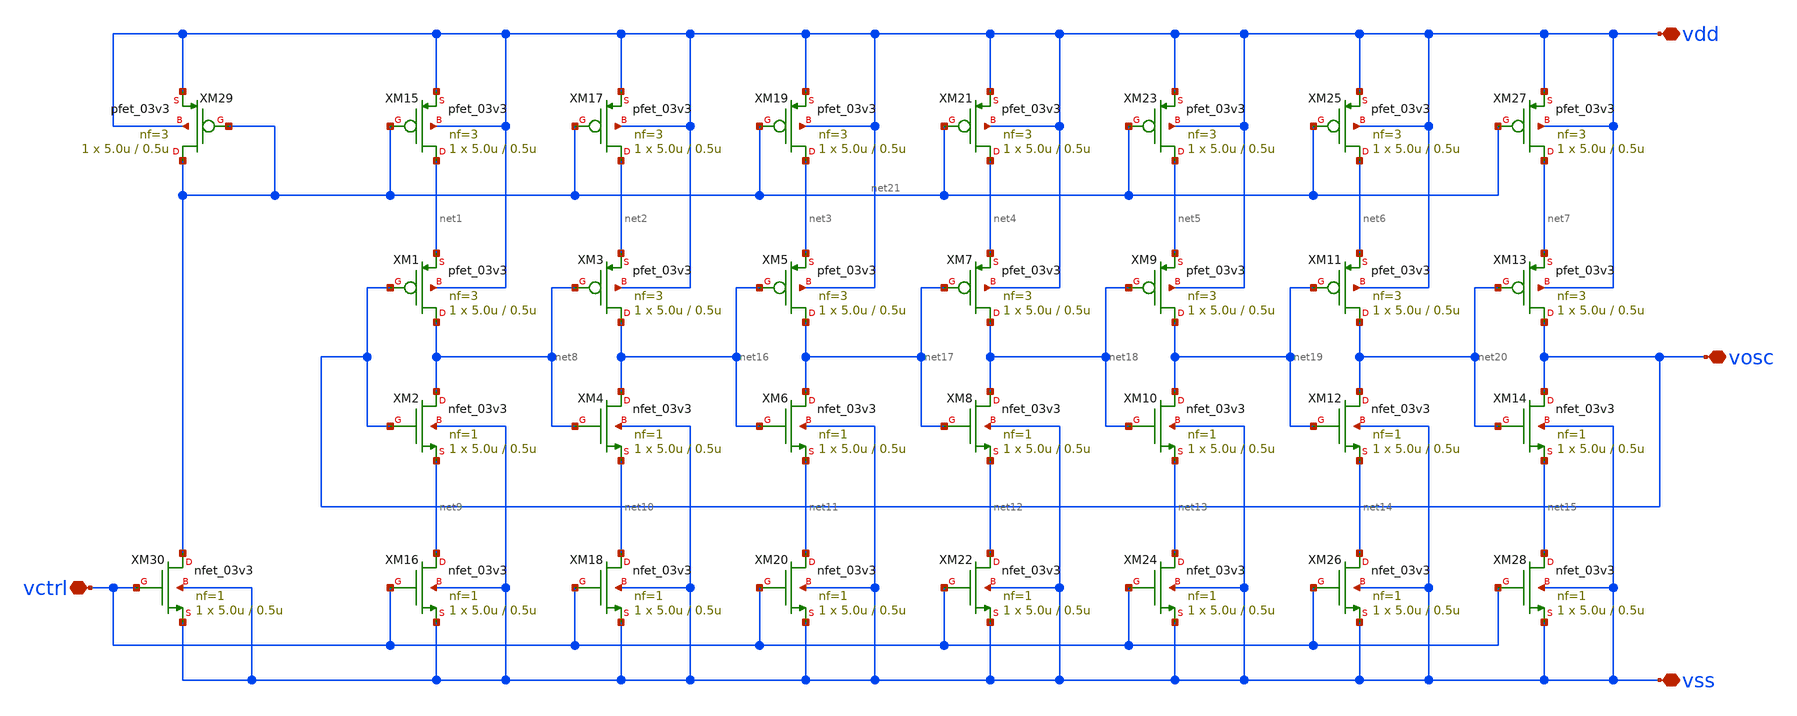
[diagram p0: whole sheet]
** sch_path: designs/libs/core_analog/CSRVCO/CSRVCO.sch
**.subckt CSRVCO vctrl vdd vss vosc
*.iopin vctrl
*.iopin vdd
*.iopin vss
*.iopin vosc
XM1 net8 vosc net1 vdd pfet_03v3 L=0.5u W=5.0u nf=3 ad='int((nf+1)/2) * W/nf * 0.18u' as='int((nf+2)/2) * W/nf * 0.18u'
+ pd='2*int((nf+1)/2) * (W/nf + 0.18u)' ps='2*int((nf+2)/2) * (W/nf + 0.18u)' nrd='0.18u / W' nrs='0.18u / W'
+ sa=0 sb=0 sd=0 m=1
XM2 net8 vosc net9 vss nfet_03v3 L=0.5u W=5.0u nf=1 ad='int((nf+1)/2) * W/nf * 0.18u' as='int((nf+2)/2) * W/nf * 0.18u'
+ pd='2*int((nf+1)/2) * (W/nf + 0.18u)' ps='2*int((nf+2)/2) * (W/nf + 0.18u)' nrd='0.18u / W' nrs='0.18u / W'
+ sa=0 sb=0 sd=0 m=1
XM3 net16 net8 net2 vdd pfet_03v3 L=0.5u W=5.0u nf=3 ad='int((nf+1)/2) * W/nf * 0.18u' as='int((nf+2)/2) * W/nf * 0.18u'
+ pd='2*int((nf+1)/2) * (W/nf + 0.18u)' ps='2*int((nf+2)/2) * (W/nf + 0.18u)' nrd='0.18u / W' nrs='0.18u / W'
+ sa=0 sb=0 sd=0 m=1
XM4 net16 net8 net10 vss nfet_03v3 L=0.5u W=5.0u nf=1 ad='int((nf+1)/2) * W/nf * 0.18u' as='int((nf+2)/2) * W/nf * 0.18u'
+ pd='2*int((nf+1)/2) * (W/nf + 0.18u)' ps='2*int((nf+2)/2) * (W/nf + 0.18u)' nrd='0.18u / W' nrs='0.18u / W'
+ sa=0 sb=0 sd=0 m=1
XM5 net17 net16 net3 vdd pfet_03v3 L=0.5u W=5.0u nf=3 ad='int((nf+1)/2) * W/nf * 0.18u' as='int((nf+2)/2) * W/nf * 0.18u'
+ pd='2*int((nf+1)/2) * (W/nf + 0.18u)' ps='2*int((nf+2)/2) * (W/nf + 0.18u)' nrd='0.18u / W' nrs='0.18u / W'
+ sa=0 sb=0 sd=0 m=1
XM6 net17 net16 net11 vss nfet_03v3 L=0.5u W=5.0u nf=1 ad='int((nf+1)/2) * W/nf * 0.18u' as='int((nf+2)/2) * W/nf * 0.18u'
+ pd='2*int((nf+1)/2) * (W/nf + 0.18u)' ps='2*int((nf+2)/2) * (W/nf + 0.18u)' nrd='0.18u / W' nrs='0.18u / W'
+ sa=0 sb=0 sd=0 m=1
XM7 net18 net17 net4 vdd pfet_03v3 L=0.5u W=5.0u nf=3 ad='int((nf+1)/2) * W/nf * 0.18u' as='int((nf+2)/2) * W/nf * 0.18u'
+ pd='2*int((nf+1)/2) * (W/nf + 0.18u)' ps='2*int((nf+2)/2) * (W/nf + 0.18u)' nrd='0.18u / W' nrs='0.18u / W'
+ sa=0 sb=0 sd=0 m=1
XM8 net18 net17 net12 vss nfet_03v3 L=0.5u W=5.0u nf=1 ad='int((nf+1)/2) * W/nf * 0.18u' as='int((nf+2)/2) * W/nf * 0.18u'
+ pd='2*int((nf+1)/2) * (W/nf + 0.18u)' ps='2*int((nf+2)/2) * (W/nf + 0.18u)' nrd='0.18u / W' nrs='0.18u / W'
+ sa=0 sb=0 sd=0 m=1
XM9 net19 net18 net5 vdd pfet_03v3 L=0.5u W=5.0u nf=3 ad='int((nf+1)/2) * W/nf * 0.18u' as='int((nf+2)/2) * W/nf * 0.18u'
+ pd='2*int((nf+1)/2) * (W/nf + 0.18u)' ps='2*int((nf+2)/2) * (W/nf + 0.18u)' nrd='0.18u / W' nrs='0.18u / W'
+ sa=0 sb=0 sd=0 m=1
XM10 net19 net18 net13 vss nfet_03v3 L=0.5u W=5.0u nf=1 ad='int((nf+1)/2) * W/nf * 0.18u' as='int((nf+2)/2) * W/nf * 0.18u'
+ pd='2*int((nf+1)/2) * (W/nf + 0.18u)' ps='2*int((nf+2)/2) * (W/nf + 0.18u)' nrd='0.18u / W' nrs='0.18u / W'
+ sa=0 sb=0 sd=0 m=1
XM11 net20 net19 net6 vdd pfet_03v3 L=0.5u W=5.0u nf=3 ad='int((nf+1)/2) * W/nf * 0.18u' as='int((nf+2)/2) * W/nf * 0.18u'
+ pd='2*int((nf+1)/2) * (W/nf + 0.18u)' ps='2*int((nf+2)/2) * (W/nf + 0.18u)' nrd='0.18u / W' nrs='0.18u / W'
+ sa=0 sb=0 sd=0 m=1
XM12 net20 net19 net14 vss nfet_03v3 L=0.5u W=5.0u nf=1 ad='int((nf+1)/2) * W/nf * 0.18u' as='int((nf+2)/2) * W/nf * 0.18u'
+ pd='2*int((nf+1)/2) * (W/nf + 0.18u)' ps='2*int((nf+2)/2) * (W/nf + 0.18u)' nrd='0.18u / W' nrs='0.18u / W'
+ sa=0 sb=0 sd=0 m=1
XM13 vosc net20 net7 vdd pfet_03v3 L=0.5u W=5.0u nf=3 ad='int((nf+1)/2) * W/nf * 0.18u' as='int((nf+2)/2) * W/nf * 0.18u'
+ pd='2*int((nf+1)/2) * (W/nf + 0.18u)' ps='2*int((nf+2)/2) * (W/nf + 0.18u)' nrd='0.18u / W' nrs='0.18u / W'
+ sa=0 sb=0 sd=0 m=1
XM14 vosc net20 net15 vss nfet_03v3 L=0.5u W=5.0u nf=1 ad='int((nf+1)/2) * W/nf * 0.18u' as='int((nf+2)/2) * W/nf * 0.18u'
+ pd='2*int((nf+1)/2) * (W/nf + 0.18u)' ps='2*int((nf+2)/2) * (W/nf + 0.18u)' nrd='0.18u / W' nrs='0.18u / W'
+ sa=0 sb=0 sd=0 m=1
XM15 net1 net21 vdd vdd pfet_03v3 L=0.5u W=5.0u nf=3 ad='int((nf+1)/2) * W/nf * 0.18u' as='int((nf+2)/2) * W/nf * 0.18u'
+ pd='2*int((nf+1)/2) * (W/nf + 0.18u)' ps='2*int((nf+2)/2) * (W/nf + 0.18u)' nrd='0.18u / W' nrs='0.18u / W'
+ sa=0 sb=0 sd=0 m=1
XM16 net9 vctrl vss vss nfet_03v3 L=0.5u W=5.0u nf=1 ad='int((nf+1)/2) * W/nf * 0.18u' as='int((nf+2)/2) * W/nf * 0.18u'
+ pd='2*int((nf+1)/2) * (W/nf + 0.18u)' ps='2*int((nf+2)/2) * (W/nf + 0.18u)' nrd='0.18u / W' nrs='0.18u / W'
+ sa=0 sb=0 sd=0 m=1
XM17 net2 net21 vdd vdd pfet_03v3 L=0.5u W=5.0u nf=3 ad='int((nf+1)/2) * W/nf * 0.18u' as='int((nf+2)/2) * W/nf * 0.18u'
+ pd='2*int((nf+1)/2) * (W/nf + 0.18u)' ps='2*int((nf+2)/2) * (W/nf + 0.18u)' nrd='0.18u / W' nrs='0.18u / W'
+ sa=0 sb=0 sd=0 m=1
XM18 net10 vctrl vss vss nfet_03v3 L=0.5u W=5.0u nf=1 ad='int((nf+1)/2) * W/nf * 0.18u' as='int((nf+2)/2) * W/nf * 0.18u'
+ pd='2*int((nf+1)/2) * (W/nf + 0.18u)' ps='2*int((nf+2)/2) * (W/nf + 0.18u)' nrd='0.18u / W' nrs='0.18u / W'
+ sa=0 sb=0 sd=0 m=1
XM19 net3 net21 vdd vdd pfet_03v3 L=0.5u W=5.0u nf=3 ad='int((nf+1)/2) * W/nf * 0.18u' as='int((nf+2)/2) * W/nf * 0.18u'
+ pd='2*int((nf+1)/2) * (W/nf + 0.18u)' ps='2*int((nf+2)/2) * (W/nf + 0.18u)' nrd='0.18u / W' nrs='0.18u / W'
+ sa=0 sb=0 sd=0 m=1
XM20 net11 vctrl vss vss nfet_03v3 L=0.5u W=5.0u nf=1 ad='int((nf+1)/2) * W/nf * 0.18u' as='int((nf+2)/2) * W/nf * 0.18u'
+ pd='2*int((nf+1)/2) * (W/nf + 0.18u)' ps='2*int((nf+2)/2) * (W/nf + 0.18u)' nrd='0.18u / W' nrs='0.18u / W'
+ sa=0 sb=0 sd=0 m=1
XM21 net4 net21 vdd vdd pfet_03v3 L=0.5u W=5.0u nf=3 ad='int((nf+1)/2) * W/nf * 0.18u' as='int((nf+2)/2) * W/nf * 0.18u'
+ pd='2*int((nf+1)/2) * (W/nf + 0.18u)' ps='2*int((nf+2)/2) * (W/nf + 0.18u)' nrd='0.18u / W' nrs='0.18u / W'
+ sa=0 sb=0 sd=0 m=1
XM22 net12 vctrl vss vss nfet_03v3 L=0.5u W=5.0u nf=1 ad='int((nf+1)/2) * W/nf * 0.18u' as='int((nf+2)/2) * W/nf * 0.18u'
+ pd='2*int((nf+1)/2) * (W/nf + 0.18u)' ps='2*int((nf+2)/2) * (W/nf + 0.18u)' nrd='0.18u / W' nrs='0.18u / W'
+ sa=0 sb=0 sd=0 m=1
XM23 net5 net21 vdd vdd pfet_03v3 L=0.5u W=5.0u nf=3 ad='int((nf+1)/2) * W/nf * 0.18u' as='int((nf+2)/2) * W/nf * 0.18u'
+ pd='2*int((nf+1)/2) * (W/nf + 0.18u)' ps='2*int((nf+2)/2) * (W/nf + 0.18u)' nrd='0.18u / W' nrs='0.18u / W'
+ sa=0 sb=0 sd=0 m=1
XM24 net13 vctrl vss vss nfet_03v3 L=0.5u W=5.0u nf=1 ad='int((nf+1)/2) * W/nf * 0.18u' as='int((nf+2)/2) * W/nf * 0.18u'
+ pd='2*int((nf+1)/2) * (W/nf + 0.18u)' ps='2*int((nf+2)/2) * (W/nf + 0.18u)' nrd='0.18u / W' nrs='0.18u / W'
+ sa=0 sb=0 sd=0 m=1
XM25 net6 net21 vdd vdd pfet_03v3 L=0.5u W=5.0u nf=3 ad='int((nf+1)/2) * W/nf * 0.18u' as='int((nf+2)/2) * W/nf * 0.18u'
+ pd='2*int((nf+1)/2) * (W/nf + 0.18u)' ps='2*int((nf+2)/2) * (W/nf + 0.18u)' nrd='0.18u / W' nrs='0.18u / W'
+ sa=0 sb=0 sd=0 m=1
XM26 net14 vctrl vss vss nfet_03v3 L=0.5u W=5.0u nf=1 ad='int((nf+1)/2) * W/nf * 0.18u' as='int((nf+2)/2) * W/nf * 0.18u'
+ pd='2*int((nf+1)/2) * (W/nf + 0.18u)' ps='2*int((nf+2)/2) * (W/nf + 0.18u)' nrd='0.18u / W' nrs='0.18u / W'
+ sa=0 sb=0 sd=0 m=1
XM27 net7 net21 vdd vdd pfet_03v3 L=0.5u W=5.0u nf=3 ad='int((nf+1)/2) * W/nf * 0.18u' as='int((nf+2)/2) * W/nf * 0.18u'
+ pd='2*int((nf+1)/2) * (W/nf + 0.18u)' ps='2*int((nf+2)/2) * (W/nf + 0.18u)' nrd='0.18u / W' nrs='0.18u / W'
+ sa=0 sb=0 sd=0 m=1
XM28 net15 vctrl vss vss nfet_03v3 L=0.5u W=5.0u nf=1 ad='int((nf+1)/2) * W/nf * 0.18u' as='int((nf+2)/2) * W/nf * 0.18u'
+ pd='2*int((nf+1)/2) * (W/nf + 0.18u)' ps='2*int((nf+2)/2) * (W/nf + 0.18u)' nrd='0.18u / W' nrs='0.18u / W'
+ sa=0 sb=0 sd=0 m=1
XM29 net21 net21 vdd vdd pfet_03v3 L=0.5u W=5.0u nf=3 ad='int((nf+1)/2) * W/nf * 0.18u' as='int((nf+2)/2) * W/nf * 0.18u'
+ pd='2*int((nf+1)/2) * (W/nf + 0.18u)' ps='2*int((nf+2)/2) * (W/nf + 0.18u)' nrd='0.18u / W' nrs='0.18u / W'
+ sa=0 sb=0 sd=0 m=1
XM30 net21 vctrl vss vss nfet_03v3 L=0.5u W=5.0u nf=1 ad='int((nf+1)/2) * W/nf * 0.18u' as='int((nf+2)/2) * W/nf * 0.18u'
+ pd='2*int((nf+1)/2) * (W/nf + 0.18u)' ps='2*int((nf+2)/2) * (W/nf + 0.18u)' nrd='0.18u / W' nrs='0.18u / W'
+ sa=0 sb=0 sd=0 m=1
**.ends
.end
